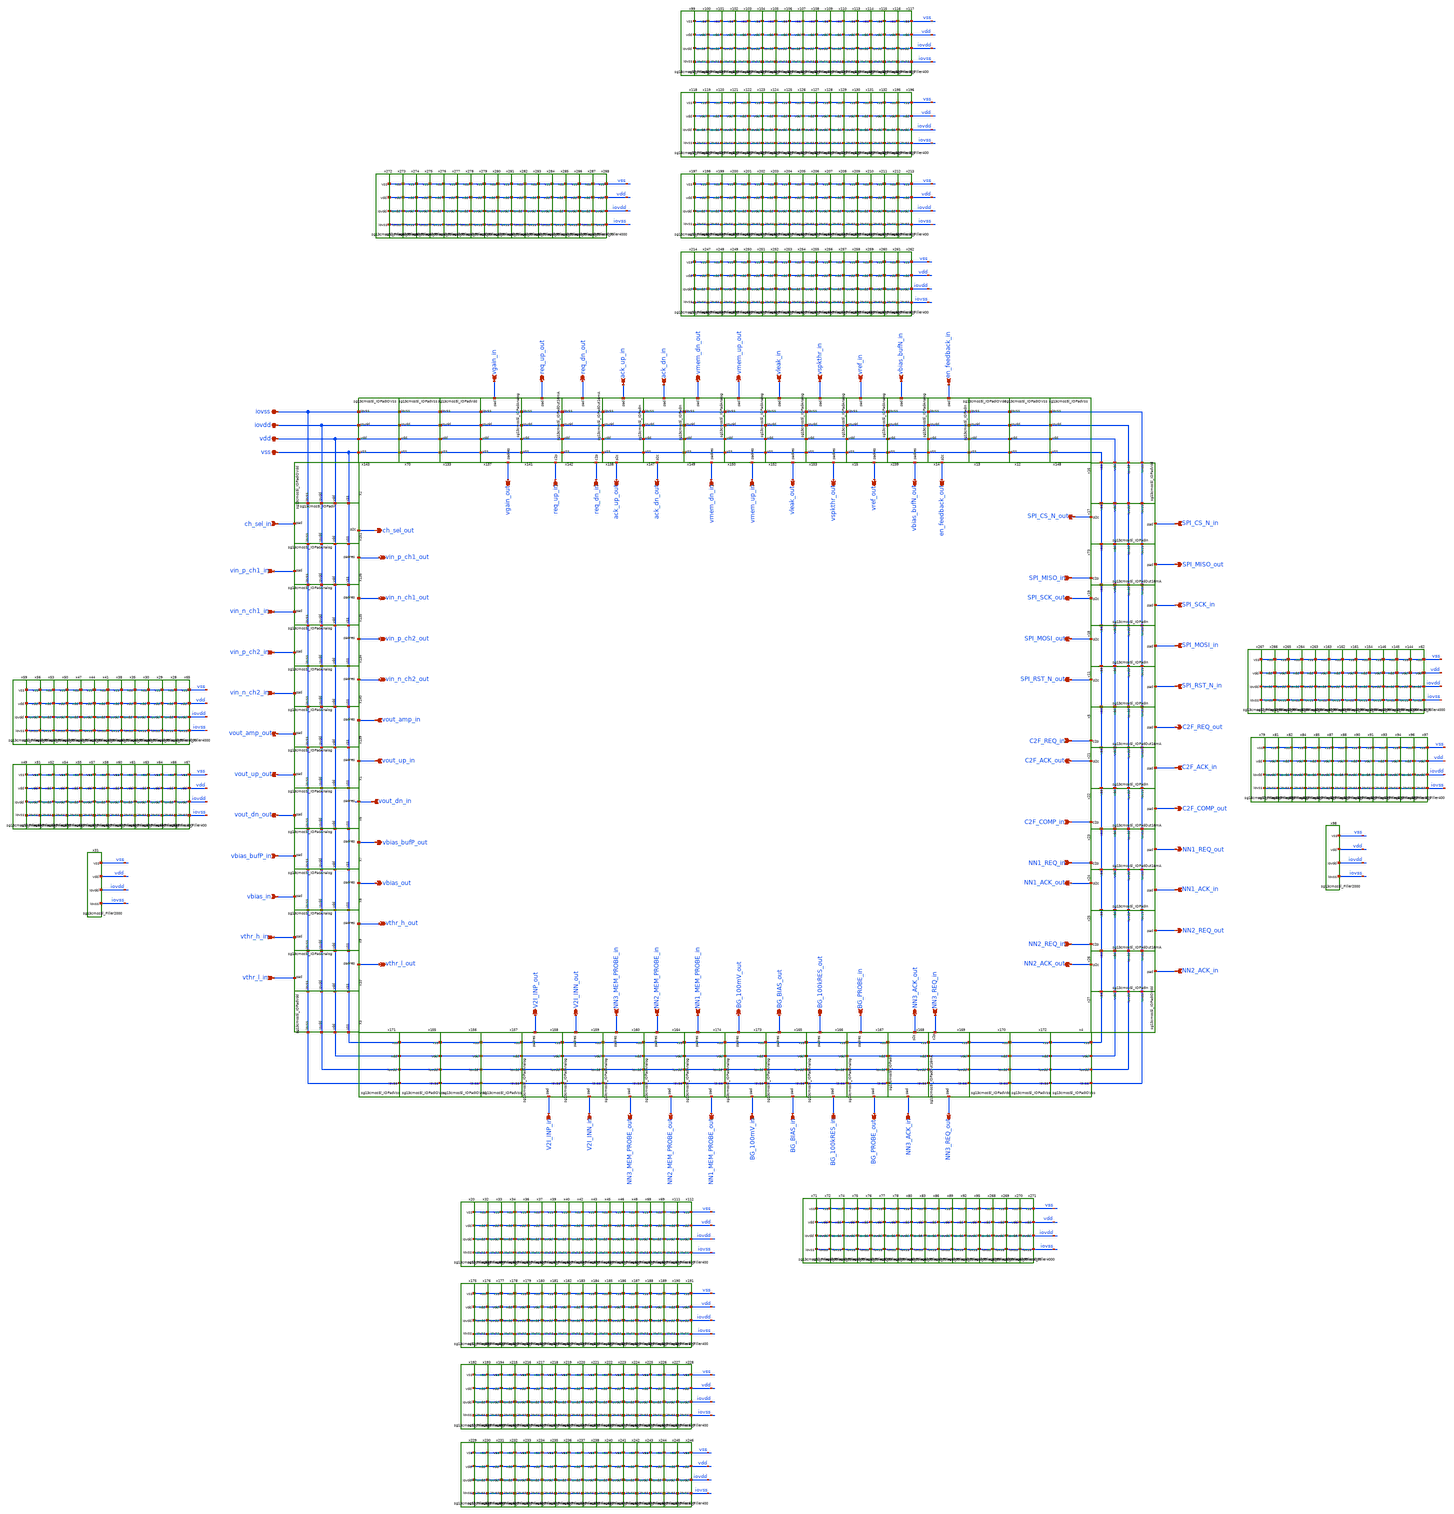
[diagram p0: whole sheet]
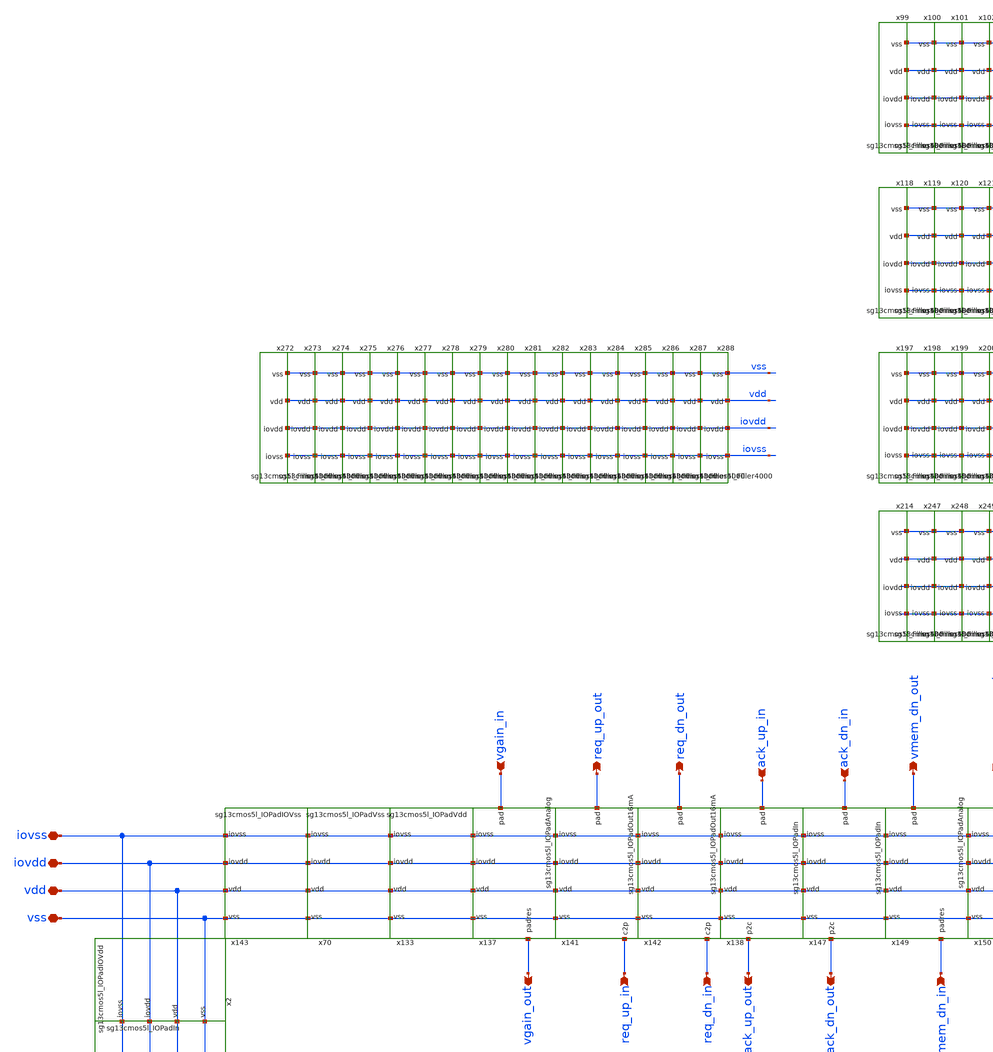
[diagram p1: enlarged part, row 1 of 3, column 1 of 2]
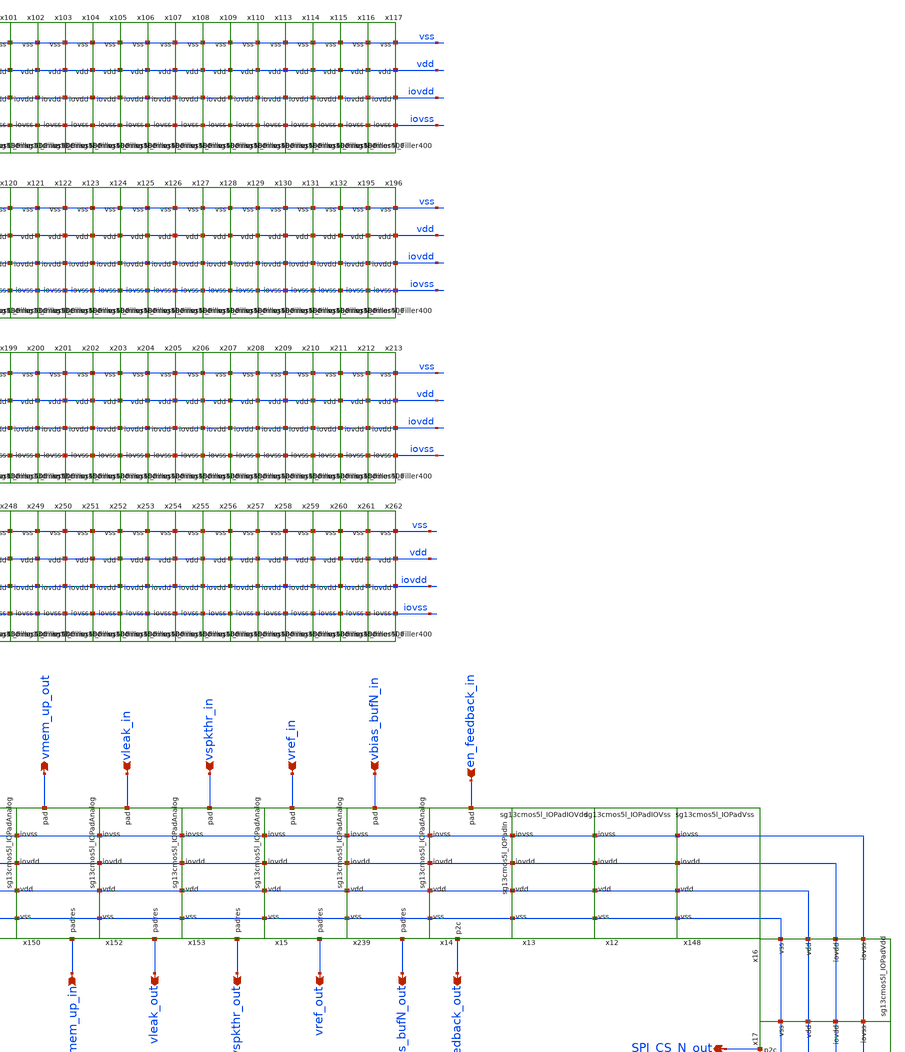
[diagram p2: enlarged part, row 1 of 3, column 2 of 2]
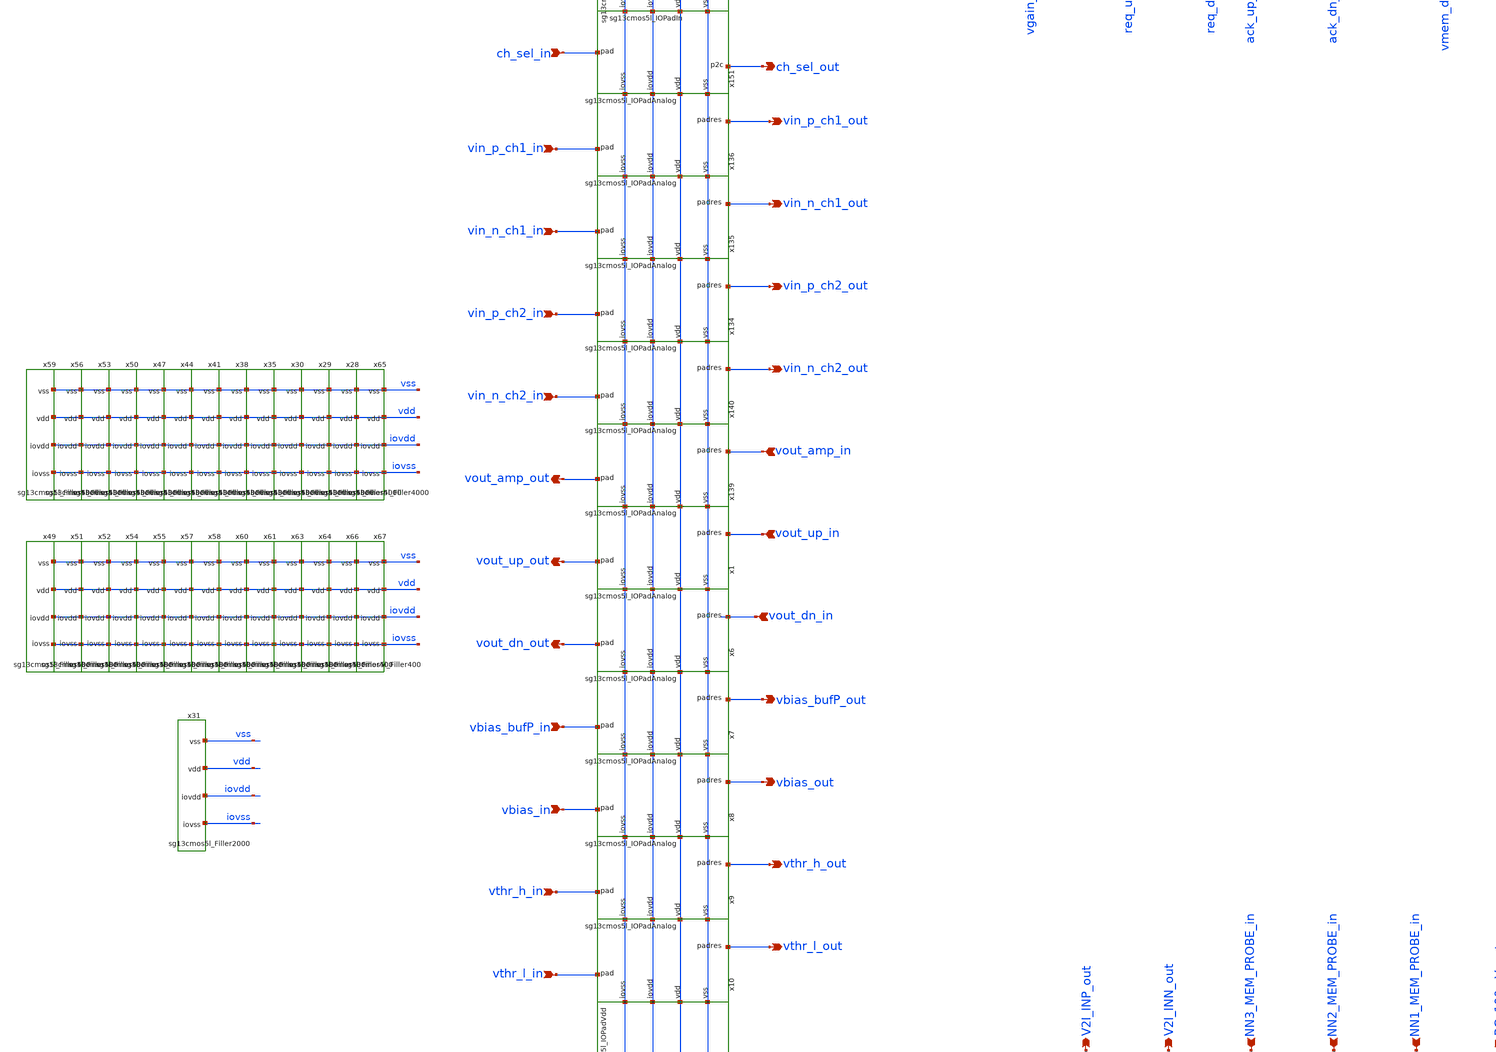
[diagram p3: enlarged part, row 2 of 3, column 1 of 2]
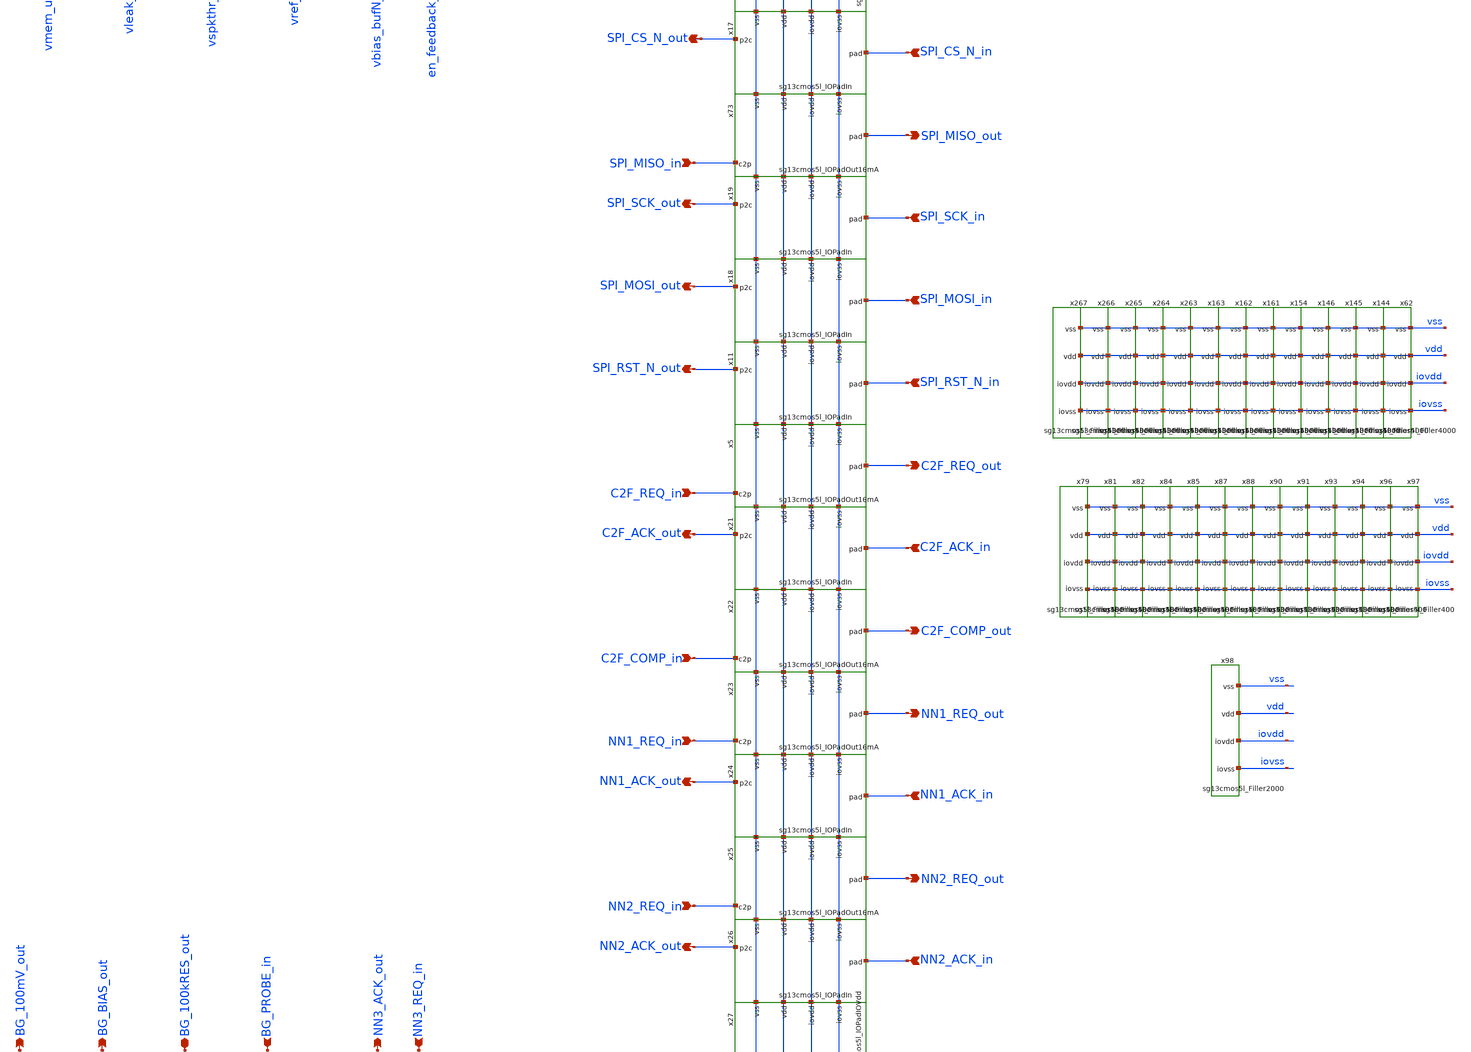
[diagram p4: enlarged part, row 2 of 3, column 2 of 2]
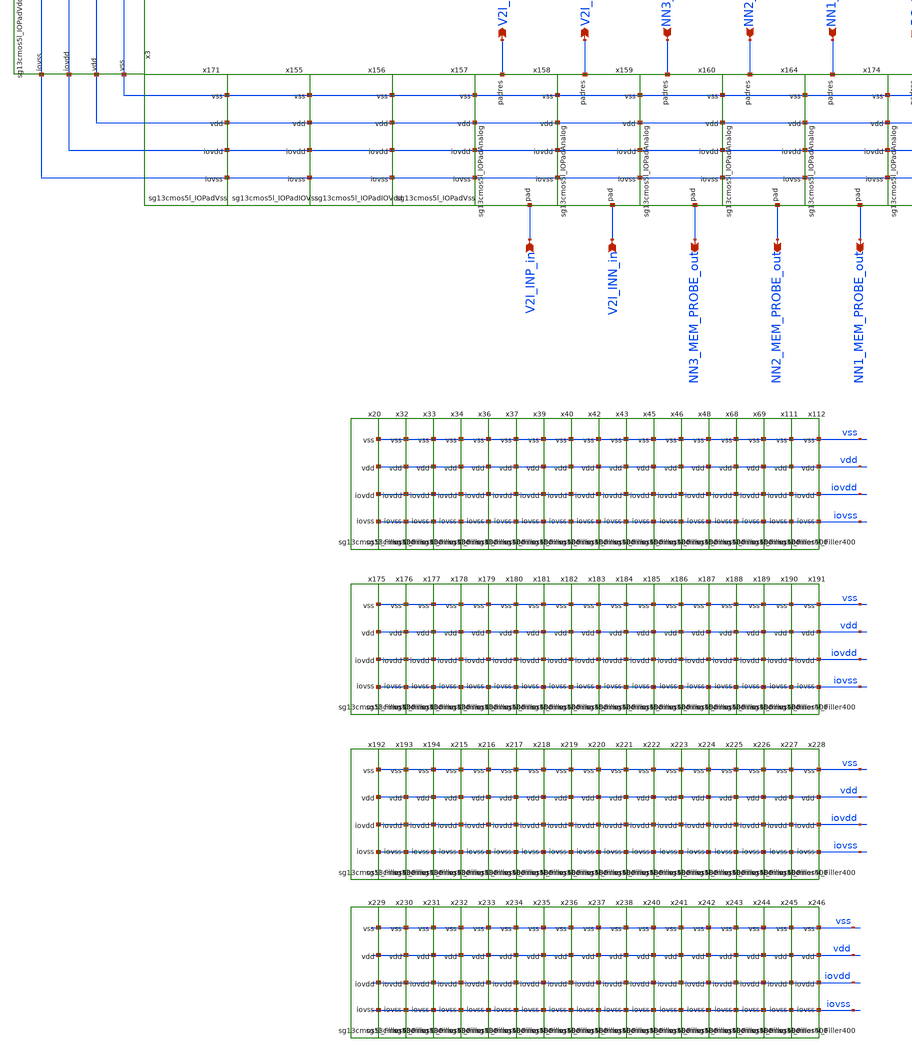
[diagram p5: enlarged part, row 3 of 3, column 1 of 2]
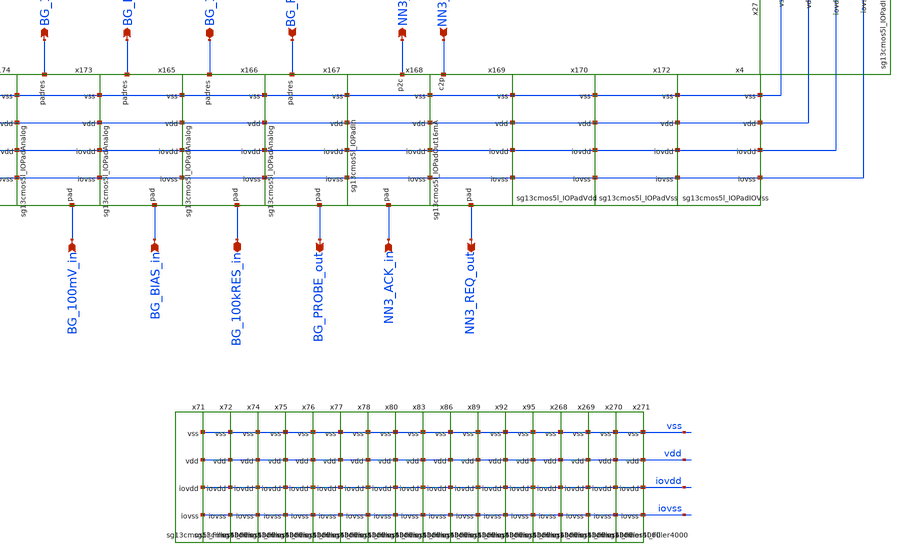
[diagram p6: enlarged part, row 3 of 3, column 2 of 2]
** sch_path: v2_feature_extr_withf/padframe_withf.sch
**.subckt padframe_withf iovss iovdd vdd vss vin_p_ch1_in vin_n_ch1_in vin_p_ch2_in vin_n_ch2_in
*+ vin_p_ch1_out vin_n_ch1_out vin_p_ch2_out vin_n_ch2_out vthr_h_in vthr_l_in vthr_h_out vthr_l_out vout_amp_in
*+ vout_up_in vout_dn_in vout_amp_out vout_up_out vout_dn_out ch_sel_in ch_sel_out vbias_in vbias_out
*+ vbias_bufN_in vbias_bufN_out vbias_bufP_in vbias_bufP_out vgain_in vleak_in vspkthr_in vref_in vgain_out
*+ vleak_out vspkthr_out vref_out vmem_up_in vmem_dn_in req_up_in req_dn_in vmem_up_out vmem_dn_out req_up_out
*+ req_dn_out ack_up_in ack_up_out ack_dn_in ack_dn_out V2I_INP_in V2I_INN_in NN3_MEM_PROBE_in NN2_MEM_PROBE_in
*+ NN1_MEM_PROBE_in BG_100mV_in BG_BIAS_in BG_100kRES_in BG_PROBE_in NN3_ACK_in NN3_REQ_in V2I_INP_out V2I_INN_out
*+ NN3_MEM_PROBE_out NN2_MEM_PROBE_out NN1_MEM_PROBE_out BG_100mV_out BG_BIAS_out BG_100kRES_out BG_PROBE_out
*+ NN3_ACK_out NN3_REQ_out NN2_ACK_in NN1_ACK_in NN2_REQ_in NN1_REQ_in C2F_COMP_in C2F_ACK_in C2F_REQ_in
*+ SPI_RST_N_in SPI_MOSI_in SPI_SCK_in SPI_CS_N_in SPI_MISO_in NN2_ACK_out NN1_ACK_out NN2_REQ_out NN1_REQ_out
*+ C2F_COMP_out C2F_ACK_out C2F_REQ_out SPI_RST_N_out SPI_MOSI_out SPI_SCK_out SPI_MISO_out SPI_CS_N_out
*+ en_feedback_in en_feedback_out
*.iopin iovss
*.iopin iovdd
*.iopin vdd
*.iopin vss
*.ipin vin_p_ch1_in
*.ipin vin_n_ch1_in
*.ipin vin_p_ch2_in
*.ipin vin_n_ch2_in
*.opin vin_p_ch1_out
*.opin vin_n_ch1_out
*.opin vin_p_ch2_out
*.opin vin_n_ch2_out
*.ipin vthr_h_in
*.ipin vthr_l_in
*.opin vthr_h_out
*.opin vthr_l_out
*.ipin vout_amp_in
*.ipin vout_up_in
*.ipin vout_dn_in
*.opin vout_amp_out
*.opin vout_up_out
*.opin vout_dn_out
*.ipin ch_sel_in
*.opin ch_sel_out
*.ipin vbias_in
*.opin vbias_out
*.ipin vbias_bufN_in
*.opin vbias_bufN_out
*.ipin vbias_bufP_in
*.opin vbias_bufP_out
*.ipin vgain_in
*.ipin vleak_in
*.ipin vspkthr_in
*.ipin vref_in
*.opin vgain_out
*.opin vleak_out
*.opin vspkthr_out
*.opin vref_out
*.ipin vmem_up_in
*.ipin vmem_dn_in
*.ipin req_up_in
*.ipin req_dn_in
*.opin vmem_up_out
*.opin vmem_dn_out
*.opin req_up_out
*.opin req_dn_out
*.ipin ack_up_in
*.opin ack_up_out
*.ipin ack_dn_in
*.opin ack_dn_out
*.ipin V2I_INP_in
*.ipin V2I_INN_in
*.ipin NN3_MEM_PROBE_in
*.ipin NN2_MEM_PROBE_in
*.ipin NN1_MEM_PROBE_in
*.ipin BG_100mV_in
*.ipin BG_BIAS_in
*.iopin BG_100kRES_in
*.ipin BG_PROBE_in
*.ipin NN3_ACK_in
*.ipin NN3_REQ_in
*.opin V2I_INP_out
*.opin V2I_INN_out
*.opin NN3_MEM_PROBE_out
*.opin NN2_MEM_PROBE_out
*.opin NN1_MEM_PROBE_out
*.opin BG_100mV_out
*.opin BG_BIAS_out
*.iopin BG_100kRES_out
*.opin BG_PROBE_out
*.opin NN3_ACK_out
*.opin NN3_REQ_out
*.ipin NN2_ACK_in
*.ipin NN1_ACK_in
*.ipin NN2_REQ_in
*.ipin NN1_REQ_in
*.ipin C2F_COMP_in
*.ipin C2F_ACK_in
*.ipin C2F_REQ_in
*.ipin SPI_RST_N_in
*.ipin SPI_MOSI_in
*.ipin SPI_SCK_in
*.ipin SPI_CS_N_in
*.ipin SPI_MISO_in
*.opin NN2_ACK_out
*.opin NN1_ACK_out
*.opin NN2_REQ_out
*.opin NN1_REQ_out
*.opin C2F_COMP_out
*.opin C2F_ACK_out
*.opin C2F_REQ_out
*.opin SPI_RST_N_out
*.opin SPI_MOSI_out
*.opin SPI_SCK_out
*.opin SPI_MISO_out
*.opin SPI_CS_N_out
*.ipin en_feedback_in
*.opin en_feedback_out
x1 iovdd iovss vout_up_out vout_up_in vdd vss sg13cmos5l_IOPadAnalog
x6 iovdd iovss vout_dn_out vout_dn_in vdd vss sg13cmos5l_IOPadAnalog
x7 iovdd iovss vbias_bufP_in vbias_bufP_out vdd vss sg13cmos5l_IOPadAnalog
x8 iovdd iovss vbias_in vbias_out vdd vss sg13cmos5l_IOPadAnalog
x9 iovdd iovss vthr_h_in vthr_h_out vdd vss sg13cmos5l_IOPadAnalog
x10 iovdd iovss vthr_l_in vthr_l_out vdd vss sg13cmos5l_IOPadAnalog
x16 iovdd iovss vdd vss sg13cmos5l_IOPadVdd
x17 iovdd iovss SPI_CS_N_out SPI_CS_N_in vdd vss sg13cmos5l_IOPadIn
x18 iovdd iovss SPI_MOSI_out SPI_MOSI_in vdd vss sg13cmos5l_IOPadIn
x19 iovdd iovss SPI_SCK_out SPI_SCK_in vdd vss sg13cmos5l_IOPadIn
x25 NN2_REQ_in iovdd iovss NN2_REQ_out vdd vss sg13cmos5l_IOPadOut16mA
x26 iovdd iovss NN2_ACK_out NN2_ACK_in vdd vss sg13cmos5l_IOPadIn
x27 iovdd iovss vdd vss sg13cmos5l_IOPadIOVdd
x21 iovdd iovss C2F_ACK_out C2F_ACK_in vdd vss sg13cmos5l_IOPadIn
x22 C2F_COMP_in iovdd iovss C2F_COMP_out vdd vss sg13cmos5l_IOPadOut16mA
x23 NN1_REQ_in iovdd iovss NN1_REQ_out vdd vss sg13cmos5l_IOPadOut16mA
x24 iovdd iovss NN1_ACK_out NN1_ACK_in vdd vss sg13cmos5l_IOPadIn
x49 iovdd iovss vdd vss sg13cmos5l_Filler400
x51 iovdd iovss vdd vss sg13cmos5l_Filler400
x52 iovdd iovss vdd vss sg13cmos5l_Filler400
x54 iovdd iovss vdd vss sg13cmos5l_Filler400
x55 iovdd iovss vdd vss sg13cmos5l_Filler400
x57 iovdd iovss vdd vss sg13cmos5l_Filler400
x58 iovdd iovss vdd vss sg13cmos5l_Filler400
x60 iovdd iovss vdd vss sg13cmos5l_Filler400
x61 iovdd iovss vdd vss sg13cmos5l_Filler400
x63 iovdd iovss vdd vss sg13cmos5l_Filler400
x64 iovdd iovss vdd vss sg13cmos5l_Filler400
x65 iovdd iovss vdd vss sg13cmos5l_Filler4000
x66 iovdd iovss vdd vss sg13cmos5l_Filler400
x67 iovdd iovss vdd vss sg13cmos5l_Filler400
x73 SPI_MISO_in iovdd iovss SPI_MISO_out vdd vss sg13cmos5l_IOPadOut16mA
x133 iovdd iovss vdd vss sg13cmos5l_IOPadVdd
x134 iovdd iovss vin_p_ch2_in vin_p_ch2_out vdd vss sg13cmos5l_IOPadAnalog
x135 iovdd iovss vin_n_ch1_in vin_n_ch1_out vdd vss sg13cmos5l_IOPadAnalog
x136 iovdd iovss vin_p_ch1_in vin_p_ch1_out vdd vss sg13cmos5l_IOPadAnalog
x139 iovdd iovss vout_amp_out vout_amp_in vdd vss sg13cmos5l_IOPadAnalog
x140 iovdd iovss vin_n_ch2_in vin_n_ch2_out vdd vss sg13cmos5l_IOPadAnalog
x141 req_up_in iovdd iovss req_up_out vdd vss sg13cmos5l_IOPadOut16mA
x142 req_dn_in iovdd iovss req_dn_out vdd vss sg13cmos5l_IOPadOut16mA
x149 iovdd iovss vmem_dn_out vmem_dn_in vdd vss sg13cmos5l_IOPadAnalog
x150 iovdd iovss vmem_up_out vmem_up_in vdd vss sg13cmos5l_IOPadAnalog
x137 iovdd iovss vgain_in vgain_out vdd vss sg13cmos5l_IOPadAnalog
x138 iovdd iovss ack_up_out ack_up_in vdd vss sg13cmos5l_IOPadIn
x147 iovdd iovss ack_dn_out ack_dn_in vdd vss sg13cmos5l_IOPadIn
x148 iovdd iovss vdd vss sg13cmos5l_IOPadVss
x152 iovdd iovss vleak_in vleak_out vdd vss sg13cmos5l_IOPadAnalog
x153 iovdd iovss vspkthr_in vspkthr_out vdd vss sg13cmos5l_IOPadAnalog
x171 iovdd iovss vdd vss sg13cmos5l_IOPadVss
x155 iovdd iovss vdd vss sg13cmos5l_IOPadIOVss
x156 iovdd iovss vdd vss sg13cmos5l_IOPadIOVdd
x157 iovdd iovss vdd vss sg13cmos5l_IOPadVss
x158 iovdd iovss V2I_INP_in V2I_INP_out vdd vss sg13cmos5l_IOPadAnalog
x159 iovdd iovss V2I_INN_in V2I_INN_out vdd vss sg13cmos5l_IOPadAnalog
x160 iovdd iovss NN3_MEM_PROBE_out NN3_MEM_PROBE_in vdd vss sg13cmos5l_IOPadAnalog
x164 iovdd iovss NN2_MEM_PROBE_out NN2_MEM_PROBE_in vdd vss sg13cmos5l_IOPadAnalog
x165 iovdd iovss BG_BIAS_in BG_BIAS_out vdd vss sg13cmos5l_IOPadAnalog
x166 iovdd iovss BG_100kRES_in BG_100kRES_out vdd vss sg13cmos5l_IOPadAnalog
x167 iovdd iovss BG_PROBE_out BG_PROBE_in vdd vss sg13cmos5l_IOPadAnalog
x168 iovdd iovss NN3_ACK_out NN3_ACK_in vdd vss sg13cmos5l_IOPadIn
x169 NN3_REQ_in iovdd iovss NN3_REQ_out vdd vss sg13cmos5l_IOPadOut16mA
x170 iovdd iovss vdd vss sg13cmos5l_IOPadVdd
x172 iovdd iovss vdd vss sg13cmos5l_IOPadVss
x173 iovdd iovss BG_100mV_in BG_100mV_out vdd vss sg13cmos5l_IOPadAnalog
x174 iovdd iovss NN1_MEM_PROBE_out NN1_MEM_PROBE_in vdd vss sg13cmos5l_IOPadAnalog
x151 iovdd iovss ch_sel_out ch_sel_in vdd vss sg13cmos5l_IOPadIn
x239 iovdd iovss vbias_bufN_in vbias_bufN_out vdd vss sg13cmos5l_IOPadAnalog
x15 iovdd iovss vref_in vref_out vdd vss sg13cmos5l_IOPadAnalog
x31 iovdd iovss vdd vss sg13cmos5l_Filler2000
x20 iovdd iovss vdd vss sg13cmos5l_Filler400
x32 iovdd iovss vdd vss sg13cmos5l_Filler400
x33 iovdd iovss vdd vss sg13cmos5l_Filler400
x34 iovdd iovss vdd vss sg13cmos5l_Filler400
x36 iovdd iovss vdd vss sg13cmos5l_Filler400
x37 iovdd iovss vdd vss sg13cmos5l_Filler400
x39 iovdd iovss vdd vss sg13cmos5l_Filler400
x40 iovdd iovss vdd vss sg13cmos5l_Filler400
x42 iovdd iovss vdd vss sg13cmos5l_Filler400
x43 iovdd iovss vdd vss sg13cmos5l_Filler400
x45 iovdd iovss vdd vss sg13cmos5l_Filler400
x46 iovdd iovss vdd vss sg13cmos5l_Filler400
x48 iovdd iovss vdd vss sg13cmos5l_Filler400
x68 iovdd iovss vdd vss sg13cmos5l_Filler400
x69 iovdd iovss vdd vss sg13cmos5l_Filler400
x111 iovdd iovss vdd vss sg13cmos5l_Filler400
x112 iovdd iovss vdd vss sg13cmos5l_Filler400
x175 iovdd iovss vdd vss sg13cmos5l_Filler400
x176 iovdd iovss vdd vss sg13cmos5l_Filler400
x177 iovdd iovss vdd vss sg13cmos5l_Filler400
x178 iovdd iovss vdd vss sg13cmos5l_Filler400
x179 iovdd iovss vdd vss sg13cmos5l_Filler400
x180 iovdd iovss vdd vss sg13cmos5l_Filler400
x181 iovdd iovss vdd vss sg13cmos5l_Filler400
x182 iovdd iovss vdd vss sg13cmos5l_Filler400
x183 iovdd iovss vdd vss sg13cmos5l_Filler400
x184 iovdd iovss vdd vss sg13cmos5l_Filler400
x185 iovdd iovss vdd vss sg13cmos5l_Filler400
x186 iovdd iovss vdd vss sg13cmos5l_Filler400
x187 iovdd iovss vdd vss sg13cmos5l_Filler400
x188 iovdd iovss vdd vss sg13cmos5l_Filler400
x189 iovdd iovss vdd vss sg13cmos5l_Filler400
x190 iovdd iovss vdd vss sg13cmos5l_Filler400
x191 iovdd iovss vdd vss sg13cmos5l_Filler400
x192 iovdd iovss vdd vss sg13cmos5l_Filler400
x193 iovdd iovss vdd vss sg13cmos5l_Filler400
x194 iovdd iovss vdd vss sg13cmos5l_Filler400
x215 iovdd iovss vdd vss sg13cmos5l_Filler400
x216 iovdd iovss vdd vss sg13cmos5l_Filler400
x217 iovdd iovss vdd vss sg13cmos5l_Filler400
x218 iovdd iovss vdd vss sg13cmos5l_Filler400
x219 iovdd iovss vdd vss sg13cmos5l_Filler400
x220 iovdd iovss vdd vss sg13cmos5l_Filler400
x221 iovdd iovss vdd vss sg13cmos5l_Filler400
x222 iovdd iovss vdd vss sg13cmos5l_Filler400
x223 iovdd iovss vdd vss sg13cmos5l_Filler400
x224 iovdd iovss vdd vss sg13cmos5l_Filler400
x225 iovdd iovss vdd vss sg13cmos5l_Filler400
x226 iovdd iovss vdd vss sg13cmos5l_Filler400
x227 iovdd iovss vdd vss sg13cmos5l_Filler400
x228 iovdd iovss vdd vss sg13cmos5l_Filler400
x229 iovdd iovss vdd vss sg13cmos5l_Filler400
x230 iovdd iovss vdd vss sg13cmos5l_Filler400
x231 iovdd iovss vdd vss sg13cmos5l_Filler400
x232 iovdd iovss vdd vss sg13cmos5l_Filler400
x233 iovdd iovss vdd vss sg13cmos5l_Filler400
x234 iovdd iovss vdd vss sg13cmos5l_Filler400
x235 iovdd iovss vdd vss sg13cmos5l_Filler400
x236 iovdd iovss vdd vss sg13cmos5l_Filler400
x237 iovdd iovss vdd vss sg13cmos5l_Filler400
x238 iovdd iovss vdd vss sg13cmos5l_Filler400
x240 iovdd iovss vdd vss sg13cmos5l_Filler400
x241 iovdd iovss vdd vss sg13cmos5l_Filler400
x242 iovdd iovss vdd vss sg13cmos5l_Filler400
x243 iovdd iovss vdd vss sg13cmos5l_Filler400
x244 iovdd iovss vdd vss sg13cmos5l_Filler400
x245 iovdd iovss vdd vss sg13cmos5l_Filler400
x246 iovdd iovss vdd vss sg13cmos5l_Filler400
x79 iovdd iovss vdd vss sg13cmos5l_Filler400
x81 iovdd iovss vdd vss sg13cmos5l_Filler400
x82 iovdd iovss vdd vss sg13cmos5l_Filler400
x84 iovdd iovss vdd vss sg13cmos5l_Filler400
x85 iovdd iovss vdd vss sg13cmos5l_Filler400
x87 iovdd iovss vdd vss sg13cmos5l_Filler400
x88 iovdd iovss vdd vss sg13cmos5l_Filler400
x90 iovdd iovss vdd vss sg13cmos5l_Filler400
x91 iovdd iovss vdd vss sg13cmos5l_Filler400
x93 iovdd iovss vdd vss sg13cmos5l_Filler400
x94 iovdd iovss vdd vss sg13cmos5l_Filler400
x96 iovdd iovss vdd vss sg13cmos5l_Filler400
x97 iovdd iovss vdd vss sg13cmos5l_Filler400
x98 iovdd iovss vdd vss sg13cmos5l_Filler2000
x99 iovdd iovss vdd vss sg13cmos5l_Filler400
x100 iovdd iovss vdd vss sg13cmos5l_Filler400
x101 iovdd iovss vdd vss sg13cmos5l_Filler400
x102 iovdd iovss vdd vss sg13cmos5l_Filler400
x103 iovdd iovss vdd vss sg13cmos5l_Filler400
x104 iovdd iovss vdd vss sg13cmos5l_Filler400
x105 iovdd iovss vdd vss sg13cmos5l_Filler400
x106 iovdd iovss vdd vss sg13cmos5l_Filler400
x107 iovdd iovss vdd vss sg13cmos5l_Filler400
x108 iovdd iovss vdd vss sg13cmos5l_Filler400
x109 iovdd iovss vdd vss sg13cmos5l_Filler400
x110 iovdd iovss vdd vss sg13cmos5l_Filler400
x113 iovdd iovss vdd vss sg13cmos5l_Filler400
x114 iovdd iovss vdd vss sg13cmos5l_Filler400
x115 iovdd iovss vdd vss sg13cmos5l_Filler400
x116 iovdd iovss vdd vss sg13cmos5l_Filler400
x117 iovdd iovss vdd vss sg13cmos5l_Filler400
x118 iovdd iovss vdd vss sg13cmos5l_Filler400
x119 iovdd iovss vdd vss sg13cmos5l_Filler400
x120 iovdd iovss vdd vss sg13cmos5l_Filler400
x121 iovdd iovss vdd vss sg13cmos5l_Filler400
x122 iovdd iovss vdd vss sg13cmos5l_Filler400
x123 iovdd iovss vdd vss sg13cmos5l_Filler400
x124 iovdd iovss vdd vss sg13cmos5l_Filler400
x125 iovdd iovss vdd vss sg13cmos5l_Filler400
x126 iovdd iovss vdd vss sg13cmos5l_Filler400
x127 iovdd iovss vdd vss sg13cmos5l_Filler400
x128 iovdd iovss vdd vss sg13cmos5l_Filler400
x129 iovdd iovss vdd vss sg13cmos5l_Filler400
x130 iovdd iovss vdd vss sg13cmos5l_Filler400
x131 iovdd iovss vdd vss sg13cmos5l_Filler400
x132 iovdd iovss vdd vss sg13cmos5l_Filler400
x195 iovdd iovss vdd vss sg13cmos5l_Filler400
x196 iovdd iovss vdd vss sg13cmos5l_Filler400
x197 iovdd iovss vdd vss sg13cmos5l_Filler400
x198 iovdd iovss vdd vss sg13cmos5l_Filler400
x199 iovdd iovss vdd vss sg13cmos5l_Filler400
x200 iovdd iovss vdd vss sg13cmos5l_Filler400
x201 iovdd iovss vdd vss sg13cmos5l_Filler400
x202 iovdd iovss vdd vss sg13cmos5l_Filler400
x203 iovdd iovss vdd vss sg13cmos5l_Filler400
x204 iovdd iovss vdd vss sg13cmos5l_Filler400
x205 iovdd iovss vdd vss sg13cmos5l_Filler400
x206 iovdd iovss vdd vss sg13cmos5l_Filler400
x207 iovdd iovss vdd vss sg13cmos5l_Filler400
x208 iovdd iovss vdd vss sg13cmos5l_Filler400
x209 iovdd iovss vdd vss sg13cmos5l_Filler400
x210 iovdd iovss vdd vss sg13cmos5l_Filler400
x211 iovdd iovss vdd vss sg13cmos5l_Filler400
x212 iovdd iovss vdd vss sg13cmos5l_Filler400
x213 iovdd iovss vdd vss sg13cmos5l_Filler400
x214 iovdd iovss vdd vss sg13cmos5l_Filler400
x247 iovdd iovss vdd vss sg13cmos5l_Filler400
x248 iovdd iovss vdd vss sg13cmos5l_Filler400
x249 iovdd iovss vdd vss sg13cmos5l_Filler400
x250 iovdd iovss vdd vss sg13cmos5l_Filler400
x251 iovdd iovss vdd vss sg13cmos5l_Filler400
x252 iovdd iovss vdd vss sg13cmos5l_Filler400
x253 iovdd iovss vdd vss sg13cmos5l_Filler400
x254 iovdd iovss vdd vss sg13cmos5l_Filler400
x255 iovdd iovss vdd vss sg13cmos5l_Filler400
x256 iovdd iovss vdd vss sg13cmos5l_Filler400
x257 iovdd iovss vdd vss sg13cmos5l_Filler400
x258 iovdd iovss vdd vss sg13cmos5l_Filler400
x259 iovdd iovss vdd vss sg13cmos5l_Filler400
x260 iovdd iovss vdd vss sg13cmos5l_Filler400
x261 iovdd iovss vdd vss sg13cmos5l_Filler400
x262 iovdd iovss vdd vss sg13cmos5l_Filler400
x2 iovdd iovss vdd vss sg13cmos5l_IOPadIOVdd
x3 iovdd iovss vdd vss sg13cmos5l_IOPadVdd
x4 iovdd iovss vdd vss sg13cmos5l_IOPadIOVss
x5 C2F_REQ_in iovdd iovss C2F_REQ_out vdd vss sg13cmos5l_IOPadOut16mA
x11 iovdd iovss SPI_RST_N_out SPI_RST_N_in vdd vss sg13cmos5l_IOPadIn
x12 iovdd iovss vdd vss sg13cmos5l_IOPadIOVss
x13 iovdd iovss vdd vss sg13cmos5l_IOPadIOVdd
x14 iovdd iovss en_feedback_out en_feedback_in vdd vss sg13cmos5l_IOPadIn
x70 iovdd iovss vdd vss sg13cmos5l_IOPadVss
x143 iovdd iovss vdd vss sg13cmos5l_IOPadIOVss
x28 iovdd iovss vdd vss sg13cmos5l_Filler4000
x29 iovdd iovss vdd vss sg13cmos5l_Filler4000
x30 iovdd iovss vdd vss sg13cmos5l_Filler4000
x35 iovdd iovss vdd vss sg13cmos5l_Filler4000
x38 iovdd iovss vdd vss sg13cmos5l_Filler4000
x41 iovdd iovss vdd vss sg13cmos5l_Filler4000
x44 iovdd iovss vdd vss sg13cmos5l_Filler4000
x47 iovdd iovss vdd vss sg13cmos5l_Filler4000
x50 iovdd iovss vdd vss sg13cmos5l_Filler4000
x53 iovdd iovss vdd vss sg13cmos5l_Filler4000
x56 iovdd iovss vdd vss sg13cmos5l_Filler4000
x59 iovdd iovss vdd vss sg13cmos5l_Filler4000
x62 iovdd iovss vdd vss sg13cmos5l_Filler4000
x144 iovdd iovss vdd vss sg13cmos5l_Filler4000
x145 iovdd iovss vdd vss sg13cmos5l_Filler4000
x146 iovdd iovss vdd vss sg13cmos5l_Filler4000
x154 iovdd iovss vdd vss sg13cmos5l_Filler4000
x161 iovdd iovss vdd vss sg13cmos5l_Filler4000
x162 iovdd iovss vdd vss sg13cmos5l_Filler4000
x163 iovdd iovss vdd vss sg13cmos5l_Filler4000
x263 iovdd iovss vdd vss sg13cmos5l_Filler4000
x264 iovdd iovss vdd vss sg13cmos5l_Filler4000
x265 iovdd iovss vdd vss sg13cmos5l_Filler4000
x266 iovdd iovss vdd vss sg13cmos5l_Filler4000
x267 iovdd iovss vdd vss sg13cmos5l_Filler4000
x71 iovdd iovss vdd vss sg13cmos5l_Filler4000
x72 iovdd iovss vdd vss sg13cmos5l_Filler4000
x74 iovdd iovss vdd vss sg13cmos5l_Filler4000
x75 iovdd iovss vdd vss sg13cmos5l_Filler4000
x76 iovdd iovss vdd vss sg13cmos5l_Filler4000
x77 iovdd iovss vdd vss sg13cmos5l_Filler4000
x78 iovdd iovss vdd vss sg13cmos5l_Filler4000
x80 iovdd iovss vdd vss sg13cmos5l_Filler4000
x83 iovdd iovss vdd vss sg13cmos5l_Filler4000
x86 iovdd iovss vdd vss sg13cmos5l_Filler4000
x89 iovdd iovss vdd vss sg13cmos5l_Filler4000
x92 iovdd iovss vdd vss sg13cmos5l_Filler4000
x95 iovdd iovss vdd vss sg13cmos5l_Filler4000
x268 iovdd iovss vdd vss sg13cmos5l_Filler4000
x269 iovdd iovss vdd vss sg13cmos5l_Filler4000
x270 iovdd iovss vdd vss sg13cmos5l_Filler4000
x271 iovdd iovss vdd vss sg13cmos5l_Filler4000
x272 iovdd iovss vdd vss sg13cmos5l_Filler4000
x273 iovdd iovss vdd vss sg13cmos5l_Filler4000
x274 iovdd iovss vdd vss sg13cmos5l_Filler4000
x275 iovdd iovss vdd vss sg13cmos5l_Filler4000
x276 iovdd iovss vdd vss sg13cmos5l_Filler4000
x277 iovdd iovss vdd vss sg13cmos5l_Filler4000
x278 iovdd iovss vdd vss sg13cmos5l_Filler4000
x279 iovdd iovss vdd vss sg13cmos5l_Filler4000
x280 iovdd iovss vdd vss sg13cmos5l_Filler4000
x281 iovdd iovss vdd vss sg13cmos5l_Filler4000
x282 iovdd iovss vdd vss sg13cmos5l_Filler4000
x283 iovdd iovss vdd vss sg13cmos5l_Filler4000
x284 iovdd iovss vdd vss sg13cmos5l_Filler4000
x285 iovdd iovss vdd vss sg13cmos5l_Filler4000
x286 iovdd iovss vdd vss sg13cmos5l_Filler4000
x287 iovdd iovss vdd vss sg13cmos5l_Filler4000
x288 iovdd iovss vdd vss sg13cmos5l_Filler4000
**.ends

* expanding   symbol:  sg13cmos5l_IOPadAnalog.sym # of pins=6
** sym_path: v2_feature_extr/sg13cmos5l_IOPadAnalog.sym
.include /foss/pdks/ihp-sg13cmos5l/libs.ref/sg13cmos5l_io/cdl/sg13cmos5l_io.cdl

* expanding   symbol:  sg13cmos5l_IOPadVdd.sym # of pins=4
** sym_path: v2_feature_extr/sg13cmos5l_IOPadVdd.sym
.include /foss/pdks/ihp-sg13cmos5l/libs.ref/sg13cmos5l_io/cdl/sg13cmos5l_io.cdl

* expanding   symbol:  sg13cmos5l_IOPadIn.sym # of pins=6
** sym_path: v2_feature_extr/sg13cmos5l_IOPadIn.sym
.include /foss/pdks/ihp-sg13cmos5l/libs.ref/sg13cmos5l_io/cdl/sg13cmos5l_io.cdl

* expanding   symbol:  sg13cmos5l_IOPadOut16mA.sym # of pins=6
** sym_path: v2_feature_extr/sg13cmos5l_IOPadOut16mA.sym
.include /foss/pdks/ihp-sg13cmos5l/libs.ref/sg13cmos5l_io/cdl/sg13cmos5l_io.cdl

* expanding   symbol:  sg13cmos5l_IOPadIOVdd.sym # of pins=4
** sym_path: v2_feature_extr_withf/sg13cmos5l_IOPadIOVdd.sym
.include /foss/pdks/ihp-sg13cmos5l/libs.ref/sg13cmos5l_io/cdl/sg13cmos5l_io.cdl

* expanding   symbol:  sg13cmos5l_Filler400.sym # of pins=4
** sym_path: v2_feature_extr_withf/sg13cmos5l_Filler400.sym
.include /foss/pdks/ihp-sg13cmos5l/libs.ref/sg13cmos5l_io/cdl/sg13cmos5l_io.cdl

* expanding   symbol:  sg13cmos5l_Filler4000.sym # of pins=4
** sym_path: v2_feature_extr_withf/sg13cmos5l_Filler4000.sym
.include /foss/pdks/ihp-sg13cmos5l/libs.ref/sg13cmos5l_io/cdl/sg13cmos5l_io.cdl

* expanding   symbol:  sg13cmos5l_IOPadVss.sym # of pins=4
** sym_path: v2_feature_extr/sg13cmos5l_IOPadVss.sym
.include /foss/pdks/ihp-sg13cmos5l/libs.ref/sg13cmos5l_io/cdl/sg13cmos5l_io.cdl

* expanding   symbol:  sg13cmos5l_IOPadIOVss.sym # of pins=4
** sym_path: v2_feature_extr/sg13cmos5l_IOPadIOVss.sym
.include /foss/pdks/ihp-sg13cmos5l/libs.ref/sg13cmos5l_io/cdl/sg13cmos5l_io.cdl

* expanding   symbol:  sg13cmos5l_Filler2000.sym # of pins=4
** sym_path: v2_feature_extr/sg13cmos5l_Filler2000.sym
.include /foss/pdks/ihp-sg13cmos5l/libs.ref/sg13cmos5l_io/cdl/sg13cmos5l_io.cdl
.end
